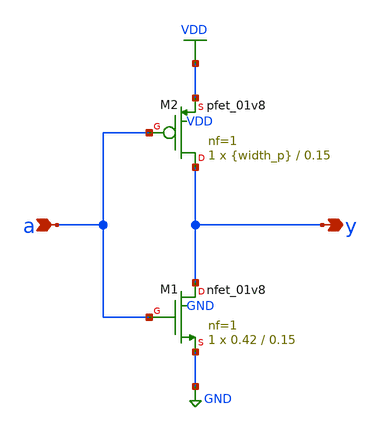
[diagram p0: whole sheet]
** sch_path: assignments/assignment3/inverter.sch
**.subckt inverter a y
*.ipin a
*.opin y
XM1 y a GND GND sky130_fd_pr__nfet_01v8 L=0.15 W=0.42 nf=1 ad='int((nf+1)/2) * W/nf * 0.29' as='int((nf+2)/2) * W/nf * 0.29'
+ pd='2*int((nf+1)/2) * (W/nf + 0.29)' ps='2*int((nf+2)/2) * (W/nf + 0.29)' nrd='0.29 / W' nrs='0.29 / W'
+ sa=0 sb=0 sd=0 mult=1 m=1
XM2 y a VDD VDD sky130_fd_pr__pfet_01v8 L=0.15 W={width_p} nf=1 ad='int((nf+1)/2) * W/nf * 0.29' as='int((nf+2)/2) * W/nf * 0.29'
+ pd='2*int((nf+1)/2) * (W/nf + 0.29)' ps='2*int((nf+2)/2) * (W/nf + 0.29)' nrd='0.29 / W' nrs='0.29 / W'
+ sa=0 sb=0 sd=0 mult=1 m=1
**.ends
.GLOBAL VDD
.GLOBAL GND
.end
